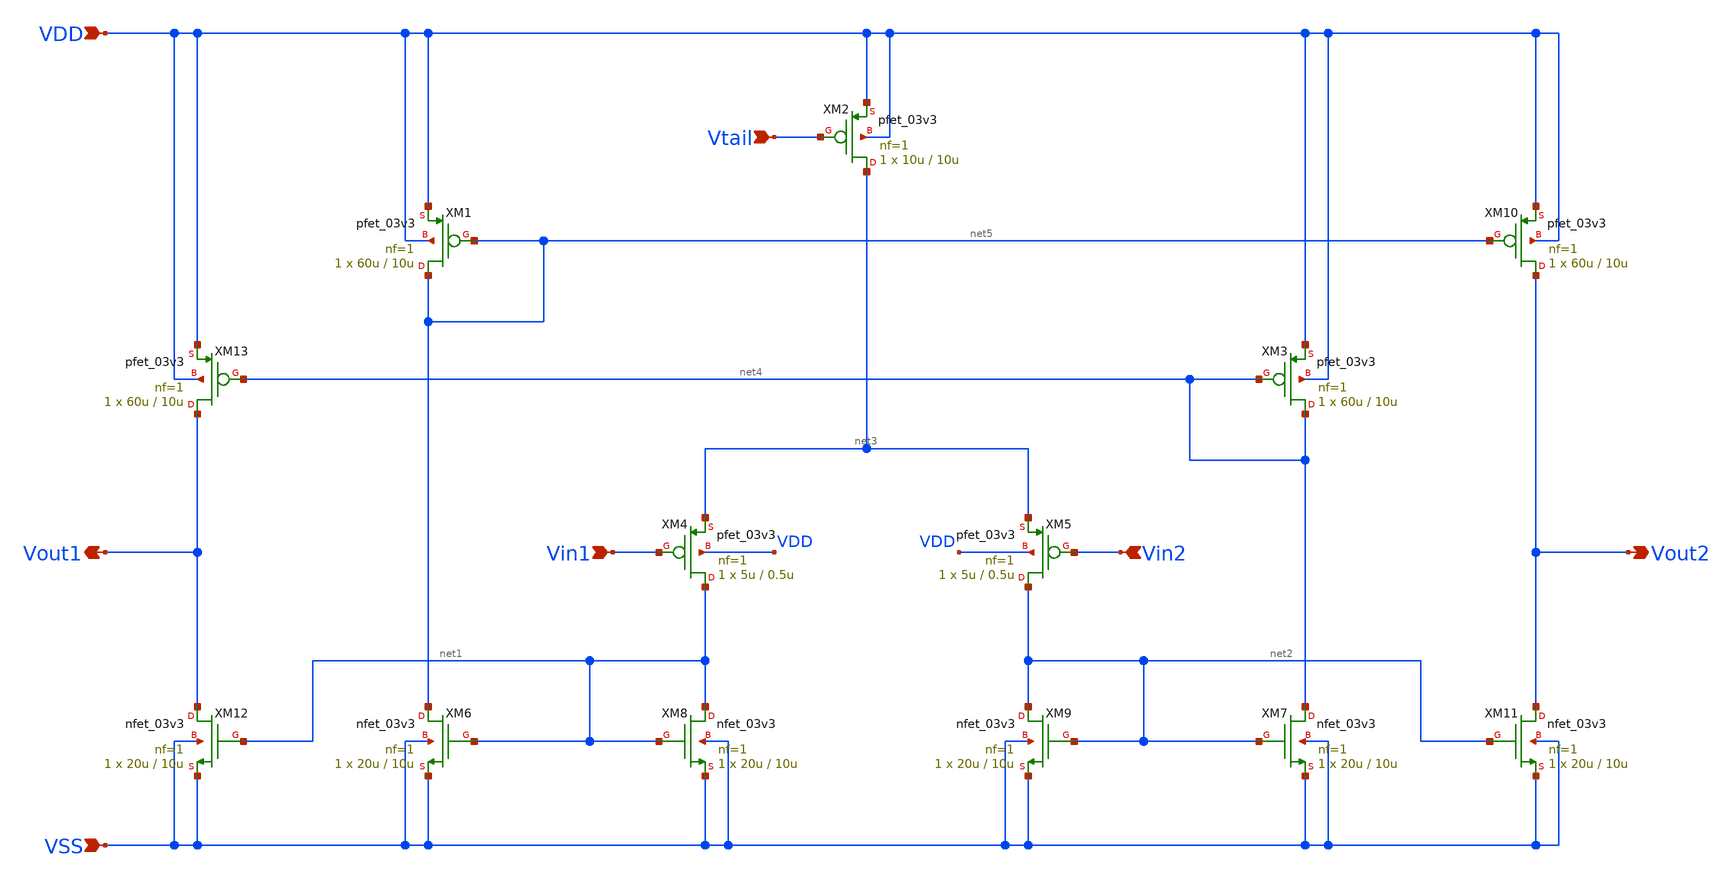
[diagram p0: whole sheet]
** sch_path: designs/libs/core_ina/ina_ota/ina_ota.sch
**.subckt ina_ota Vin1 Vin2 Vtail VSS Vout2 VDD Vout1
*.ipin Vin1
*.ipin Vin2
*.ipin Vtail
*.ipin VSS
*.opin Vout2
*.ipin VDD
*.opin Vout1
XM1 net5 net5 VDD VDD pfet_03v3 L=10u W=60u nf=1 ad='int((nf+1)/2) * W/nf * 0.18u' as='int((nf+2)/2) * W/nf * 0.18u'
+ pd='2*int((nf+1)/2) * (W/nf + 0.18u)' ps='2*int((nf+2)/2) * (W/nf + 0.18u)' nrd='0.18u / W' nrs='0.18u / W'
+ sa=0 sb=0 sd=0 m=1
XM2 net3 Vtail VDD VDD pfet_03v3 L=10u W=10u nf=1 ad='int((nf+1)/2) * W/nf * 0.18u' as='int((nf+2)/2) * W/nf * 0.18u'
+ pd='2*int((nf+1)/2) * (W/nf + 0.18u)' ps='2*int((nf+2)/2) * (W/nf + 0.18u)' nrd='0.18u / W' nrs='0.18u / W'
+ sa=0 sb=0 sd=0 m=1
XM3 net4 net4 VDD VDD pfet_03v3 L=10u W=60u nf=1 ad='int((nf+1)/2) * W/nf * 0.18u' as='int((nf+2)/2) * W/nf * 0.18u'
+ pd='2*int((nf+1)/2) * (W/nf + 0.18u)' ps='2*int((nf+2)/2) * (W/nf + 0.18u)' nrd='0.18u / W' nrs='0.18u / W'
+ sa=0 sb=0 sd=0 m=1
XM4 net1 Vin1 net3 VDD pfet_03v3 L=0.5u W=5u nf=1 ad='int((nf+1)/2) * W/nf * 0.18u' as='int((nf+2)/2) * W/nf * 0.18u'
+ pd='2*int((nf+1)/2) * (W/nf + 0.18u)' ps='2*int((nf+2)/2) * (W/nf + 0.18u)' nrd='0.18u / W' nrs='0.18u / W'
+ sa=0 sb=0 sd=0 m=1
XM5 net2 Vin2 net3 VDD pfet_03v3 L=0.5u W=5u nf=1 ad='int((nf+1)/2) * W/nf * 0.18u' as='int((nf+2)/2) * W/nf * 0.18u'
+ pd='2*int((nf+1)/2) * (W/nf + 0.18u)' ps='2*int((nf+2)/2) * (W/nf + 0.18u)' nrd='0.18u / W' nrs='0.18u / W'
+ sa=0 sb=0 sd=0 m=1
XM6 net5 net1 VSS VSS nfet_03v3 L=10u W=20u nf=1 ad='int((nf+1)/2) * W/nf * 0.18u' as='int((nf+2)/2) * W/nf * 0.18u'
+ pd='2*int((nf+1)/2) * (W/nf + 0.18u)' ps='2*int((nf+2)/2) * (W/nf + 0.18u)' nrd='0.18u / W' nrs='0.18u / W'
+ sa=0 sb=0 sd=0 m=1
XM7 net4 net2 VSS VSS nfet_03v3 L=10u W=20u nf=1 ad='int((nf+1)/2) * W/nf * 0.18u' as='int((nf+2)/2) * W/nf * 0.18u'
+ pd='2*int((nf+1)/2) * (W/nf + 0.18u)' ps='2*int((nf+2)/2) * (W/nf + 0.18u)' nrd='0.18u / W' nrs='0.18u / W'
+ sa=0 sb=0 sd=0 m=1
XM8 net1 net1 VSS VSS nfet_03v3 L=10u W=20u nf=1 ad='int((nf+1)/2) * W/nf * 0.18u' as='int((nf+2)/2) * W/nf * 0.18u'
+ pd='2*int((nf+1)/2) * (W/nf + 0.18u)' ps='2*int((nf+2)/2) * (W/nf + 0.18u)' nrd='0.18u / W' nrs='0.18u / W'
+ sa=0 sb=0 sd=0 m=1
XM9 net2 net2 VSS VSS nfet_03v3 L=10u W=20u nf=1 ad='int((nf+1)/2) * W/nf * 0.18u' as='int((nf+2)/2) * W/nf * 0.18u'
+ pd='2*int((nf+1)/2) * (W/nf + 0.18u)' ps='2*int((nf+2)/2) * (W/nf + 0.18u)' nrd='0.18u / W' nrs='0.18u / W'
+ sa=0 sb=0 sd=0 m=1
XM10 Vout2 net5 VDD VDD pfet_03v3 L=10u W=60u nf=1 ad='int((nf+1)/2) * W/nf * 0.18u' as='int((nf+2)/2) * W/nf * 0.18u'
+ pd='2*int((nf+1)/2) * (W/nf + 0.18u)' ps='2*int((nf+2)/2) * (W/nf + 0.18u)' nrd='0.18u / W' nrs='0.18u / W'
+ sa=0 sb=0 sd=0 m=1
XM11 Vout2 net2 VSS VSS nfet_03v3 L=10u W=20u nf=1 ad='int((nf+1)/2) * W/nf * 0.18u' as='int((nf+2)/2) * W/nf * 0.18u'
+ pd='2*int((nf+1)/2) * (W/nf + 0.18u)' ps='2*int((nf+2)/2) * (W/nf + 0.18u)' nrd='0.18u / W' nrs='0.18u / W'
+ sa=0 sb=0 sd=0 m=1
XM12 Vout1 net1 VSS VSS nfet_03v3 L=10u W=20u nf=1 ad='int((nf+1)/2) * W/nf * 0.18u' as='int((nf+2)/2) * W/nf * 0.18u'
+ pd='2*int((nf+1)/2) * (W/nf + 0.18u)' ps='2*int((nf+2)/2) * (W/nf + 0.18u)' nrd='0.18u / W' nrs='0.18u / W'
+ sa=0 sb=0 sd=0 m=1
XM13 Vout1 net4 VDD VDD pfet_03v3 L=10u W=60u nf=1 ad='int((nf+1)/2) * W/nf * 0.18u' as='int((nf+2)/2) * W/nf * 0.18u'
+ pd='2*int((nf+1)/2) * (W/nf + 0.18u)' ps='2*int((nf+2)/2) * (W/nf + 0.18u)' nrd='0.18u / W' nrs='0.18u / W'
+ sa=0 sb=0 sd=0 m=1
**.ends
.end
